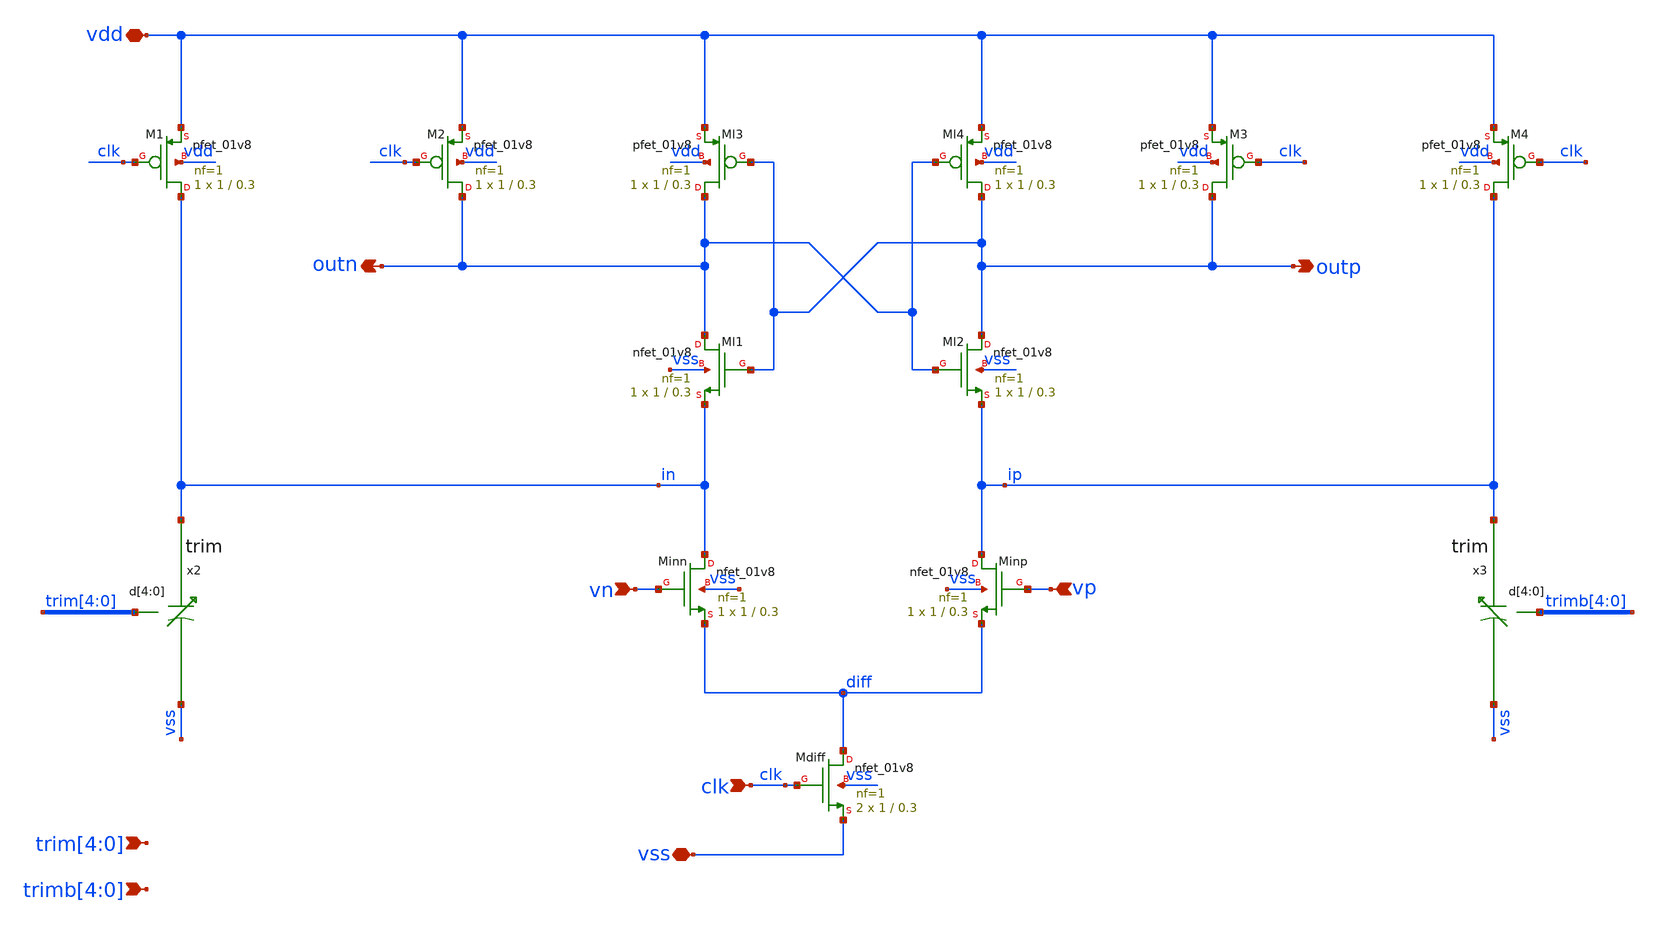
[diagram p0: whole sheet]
** sch_path: xschem/sar_10b/comparator/comparator.sch
**.subckt comparator vn vp clk vdd vss outp outn trim[4],trim[3],trim[2],trim[1],trim[0]
*+ trimb[4],trimb[3],trimb[2],trimb[1],trimb[0]
*.ipin vn
*.ipin vp
*.ipin clk
*.iopin vdd
*.iopin vss
*.opin outp
*.opin outn
*.ipin trim[4],trim[3],trim[2],trim[1],trim[0]
*.ipin trimb[4],trimb[3],trimb[2],trimb[1],trimb[0]
XMdiff diff clk vss vss sky130_fd_pr__nfet_01v8 L=0.3 W=1 nf=1 ad='int((nf+1)/2) * W/nf * 0.29' as='int((nf+2)/2) * W/nf * 0.29'
+ pd='2*int((nf+1)/2) * (W/nf + 0.29)' ps='2*int((nf+2)/2) * (W/nf + 0.29)' nrd='0.29 / W' nrs='0.29 / W'
+ sa=0 sb=0 sd=0 mult=2 m=2
XMinn in vn diff vss sky130_fd_pr__nfet_01v8 L=0.3 W=1 nf=1 ad='int((nf+1)/2) * W/nf * 0.29' as='int((nf+2)/2) * W/nf * 0.29'
+ pd='2*int((nf+1)/2) * (W/nf + 0.29)' ps='2*int((nf+2)/2) * (W/nf + 0.29)' nrd='0.29 / W' nrs='0.29 / W'
+ sa=0 sb=0 sd=0 mult=1 m=1
XMinp ip vp diff vss sky130_fd_pr__nfet_01v8 L=0.3 W=1 nf=1 ad='int((nf+1)/2) * W/nf * 0.29' as='int((nf+2)/2) * W/nf * 0.29'
+ pd='2*int((nf+1)/2) * (W/nf + 0.29)' ps='2*int((nf+2)/2) * (W/nf + 0.29)' nrd='0.29 / W' nrs='0.29 / W'
+ sa=0 sb=0 sd=0 mult=1 m=1
XMl4 outp outn vdd vdd sky130_fd_pr__pfet_01v8 L=0.3 W=1 nf=1 ad='int((nf+1)/2) * W/nf * 0.29' as='int((nf+2)/2) * W/nf * 0.29'
+ pd='2*int((nf+1)/2) * (W/nf + 0.29)' ps='2*int((nf+2)/2) * (W/nf + 0.29)' nrd='0.29 / W' nrs='0.29 / W'
+ sa=0 sb=0 sd=0 mult=1 m=1
XMl3 outn outp vdd vdd sky130_fd_pr__pfet_01v8 L=0.3 W=1 nf=1 ad='int((nf+1)/2) * W/nf * 0.29' as='int((nf+2)/2) * W/nf * 0.29'
+ pd='2*int((nf+1)/2) * (W/nf + 0.29)' ps='2*int((nf+2)/2) * (W/nf + 0.29)' nrd='0.29 / W' nrs='0.29 / W'
+ sa=0 sb=0 sd=0 mult=1 m=1
XM3 outp clk vdd vdd sky130_fd_pr__pfet_01v8 L=0.3 W=1 nf=1 ad='int((nf+1)/2) * W/nf * 0.29' as='int((nf+2)/2) * W/nf * 0.29'
+ pd='2*int((nf+1)/2) * (W/nf + 0.29)' ps='2*int((nf+2)/2) * (W/nf + 0.29)' nrd='0.29 / W' nrs='0.29 / W'
+ sa=0 sb=0 sd=0 mult=1 m=1
XM2 outn clk vdd vdd sky130_fd_pr__pfet_01v8 L=0.3 W=1 nf=1 ad='int((nf+1)/2) * W/nf * 0.29' as='int((nf+2)/2) * W/nf * 0.29'
+ pd='2*int((nf+1)/2) * (W/nf + 0.29)' ps='2*int((nf+2)/2) * (W/nf + 0.29)' nrd='0.29 / W' nrs='0.29 / W'
+ sa=0 sb=0 sd=0 mult=1 m=1
XMl1 outn outp in vss sky130_fd_pr__nfet_01v8 L=0.3 W=1 nf=1 ad='int((nf+1)/2) * W/nf * 0.29' as='int((nf+2)/2) * W/nf * 0.29'
+ pd='2*int((nf+1)/2) * (W/nf + 0.29)' ps='2*int((nf+2)/2) * (W/nf + 0.29)' nrd='0.29 / W' nrs='0.29 / W'
+ sa=0 sb=0 sd=0 mult=1 m=1
XMl2 outp outn ip vss sky130_fd_pr__nfet_01v8 L=0.3 W=1 nf=1 ad='int((nf+1)/2) * W/nf * 0.29' as='int((nf+2)/2) * W/nf * 0.29'
+ pd='2*int((nf+1)/2) * (W/nf + 0.29)' ps='2*int((nf+2)/2) * (W/nf + 0.29)' nrd='0.29 / W' nrs='0.29 / W'
+ sa=0 sb=0 sd=0 mult=1 m=1
XM4 ip clk vdd vdd sky130_fd_pr__pfet_01v8 L=0.3 W=1 nf=1 ad='int((nf+1)/2) * W/nf * 0.29' as='int((nf+2)/2) * W/nf * 0.29'
+ pd='2*int((nf+1)/2) * (W/nf + 0.29)' ps='2*int((nf+2)/2) * (W/nf + 0.29)' nrd='0.29 / W' nrs='0.29 / W'
+ sa=0 sb=0 sd=0 mult=1 m=1
XM1 in clk vdd vdd sky130_fd_pr__pfet_01v8 L=0.3 W=1 nf=1 ad='int((nf+1)/2) * W/nf * 0.29' as='int((nf+2)/2) * W/nf * 0.29'
+ pd='2*int((nf+1)/2) * (W/nf + 0.29)' ps='2*int((nf+2)/2) * (W/nf + 0.29)' nrd='0.29 / W' nrs='0.29 / W'
+ sa=0 sb=0 sd=0 mult=1 m=1
x2 in trim[4] trim[3] trim[2] trim[1] trim[0] vss trim
x3 ip trimb[4] trimb[3] trimb[2] trimb[1] trimb[0] vss trim
**.ends

* expanding   symbol:  sar_10b/comparator/trim.sym # of pins=3
** sym_path: xschem/sar_10b/comparator/trim.sym
** sch_path: xschem/sar_10b/comparator/trim.sch
.subckt trim drain d[4] d[3] d[2] d[1] d[0] vss
*.iopin vss
*.ipin d[4],d[3],d[2],d[1],d[0]
*.opin drain
XM4[7] n4 d[4] vss vss sky130_fd_pr__nfet_01v8_lvt L=0.3 W=1 nf=1 ad='int((nf+1)/2) * W/nf * 0.29' as='int((nf+2)/2) * W/nf * 0.29'
+ pd='2*int((nf+1)/2) * (W/nf + 0.29)' ps='2*int((nf+2)/2) * (W/nf + 0.29)' nrd='0.29 / W' nrs='0.29 / W'
+ sa=0 sb=0 sd=0 mult=1 m=1
XM4[6] n4 d[4] vss vss sky130_fd_pr__nfet_01v8_lvt L=0.3 W=1 nf=1 ad='int((nf+1)/2) * W/nf * 0.29' as='int((nf+2)/2) * W/nf * 0.29'
+ pd='2*int((nf+1)/2) * (W/nf + 0.29)' ps='2*int((nf+2)/2) * (W/nf + 0.29)' nrd='0.29 / W' nrs='0.29 / W'
+ sa=0 sb=0 sd=0 mult=1 m=1
XM4[5] n4 d[4] vss vss sky130_fd_pr__nfet_01v8_lvt L=0.3 W=1 nf=1 ad='int((nf+1)/2) * W/nf * 0.29' as='int((nf+2)/2) * W/nf * 0.29'
+ pd='2*int((nf+1)/2) * (W/nf + 0.29)' ps='2*int((nf+2)/2) * (W/nf + 0.29)' nrd='0.29 / W' nrs='0.29 / W'
+ sa=0 sb=0 sd=0 mult=1 m=1
XM4[4] n4 d[4] vss vss sky130_fd_pr__nfet_01v8_lvt L=0.3 W=1 nf=1 ad='int((nf+1)/2) * W/nf * 0.29' as='int((nf+2)/2) * W/nf * 0.29'
+ pd='2*int((nf+1)/2) * (W/nf + 0.29)' ps='2*int((nf+2)/2) * (W/nf + 0.29)' nrd='0.29 / W' nrs='0.29 / W'
+ sa=0 sb=0 sd=0 mult=1 m=1
XM4[3] n4 d[4] vss vss sky130_fd_pr__nfet_01v8_lvt L=0.3 W=1 nf=1 ad='int((nf+1)/2) * W/nf * 0.29' as='int((nf+2)/2) * W/nf * 0.29'
+ pd='2*int((nf+1)/2) * (W/nf + 0.29)' ps='2*int((nf+2)/2) * (W/nf + 0.29)' nrd='0.29 / W' nrs='0.29 / W'
+ sa=0 sb=0 sd=0 mult=1 m=1
XM4[2] n4 d[4] vss vss sky130_fd_pr__nfet_01v8_lvt L=0.3 W=1 nf=1 ad='int((nf+1)/2) * W/nf * 0.29' as='int((nf+2)/2) * W/nf * 0.29'
+ pd='2*int((nf+1)/2) * (W/nf + 0.29)' ps='2*int((nf+2)/2) * (W/nf + 0.29)' nrd='0.29 / W' nrs='0.29 / W'
+ sa=0 sb=0 sd=0 mult=1 m=1
XM4[1] n4 d[4] vss vss sky130_fd_pr__nfet_01v8_lvt L=0.3 W=1 nf=1 ad='int((nf+1)/2) * W/nf * 0.29' as='int((nf+2)/2) * W/nf * 0.29'
+ pd='2*int((nf+1)/2) * (W/nf + 0.29)' ps='2*int((nf+2)/2) * (W/nf + 0.29)' nrd='0.29 / W' nrs='0.29 / W'
+ sa=0 sb=0 sd=0 mult=1 m=1
XM4[0] n4 d[4] vss vss sky130_fd_pr__nfet_01v8_lvt L=0.3 W=1 nf=1 ad='int((nf+1)/2) * W/nf * 0.29' as='int((nf+2)/2) * W/nf * 0.29'
+ pd='2*int((nf+1)/2) * (W/nf + 0.29)' ps='2*int((nf+2)/2) * (W/nf + 0.29)' nrd='0.29 / W' nrs='0.29 / W'
+ sa=0 sb=0 sd=0 mult=1 m=1
XM3[3] n3 d[3] vss vss sky130_fd_pr__nfet_01v8_lvt L=0.3 W=1 nf=1 ad='int((nf+1)/2) * W/nf * 0.29' as='int((nf+2)/2) * W/nf * 0.29'
+ pd='2*int((nf+1)/2) * (W/nf + 0.29)' ps='2*int((nf+2)/2) * (W/nf + 0.29)' nrd='0.29 / W' nrs='0.29 / W'
+ sa=0 sb=0 sd=0 mult=1 m=1
XM3[2] n3 d[3] vss vss sky130_fd_pr__nfet_01v8_lvt L=0.3 W=1 nf=1 ad='int((nf+1)/2) * W/nf * 0.29' as='int((nf+2)/2) * W/nf * 0.29'
+ pd='2*int((nf+1)/2) * (W/nf + 0.29)' ps='2*int((nf+2)/2) * (W/nf + 0.29)' nrd='0.29 / W' nrs='0.29 / W'
+ sa=0 sb=0 sd=0 mult=1 m=1
XM3[1] n3 d[3] vss vss sky130_fd_pr__nfet_01v8_lvt L=0.3 W=1 nf=1 ad='int((nf+1)/2) * W/nf * 0.29' as='int((nf+2)/2) * W/nf * 0.29'
+ pd='2*int((nf+1)/2) * (W/nf + 0.29)' ps='2*int((nf+2)/2) * (W/nf + 0.29)' nrd='0.29 / W' nrs='0.29 / W'
+ sa=0 sb=0 sd=0 mult=1 m=1
XM3[0] n3 d[3] vss vss sky130_fd_pr__nfet_01v8_lvt L=0.3 W=1 nf=1 ad='int((nf+1)/2) * W/nf * 0.29' as='int((nf+2)/2) * W/nf * 0.29'
+ pd='2*int((nf+1)/2) * (W/nf + 0.29)' ps='2*int((nf+2)/2) * (W/nf + 0.29)' nrd='0.29 / W' nrs='0.29 / W'
+ sa=0 sb=0 sd=0 mult=1 m=1
XM2[1] n2 d[2] vss vss sky130_fd_pr__nfet_01v8_lvt L=0.3 W=1 nf=1 ad='int((nf+1)/2) * W/nf * 0.29' as='int((nf+2)/2) * W/nf * 0.29'
+ pd='2*int((nf+1)/2) * (W/nf + 0.29)' ps='2*int((nf+2)/2) * (W/nf + 0.29)' nrd='0.29 / W' nrs='0.29 / W'
+ sa=0 sb=0 sd=0 mult=1 m=1
XM2[0] n2 d[2] vss vss sky130_fd_pr__nfet_01v8_lvt L=0.3 W=1 nf=1 ad='int((nf+1)/2) * W/nf * 0.29' as='int((nf+2)/2) * W/nf * 0.29'
+ pd='2*int((nf+1)/2) * (W/nf + 0.29)' ps='2*int((nf+2)/2) * (W/nf + 0.29)' nrd='0.29 / W' nrs='0.29 / W'
+ sa=0 sb=0 sd=0 mult=1 m=1
XM1 n1 d[1] vss vss sky130_fd_pr__nfet_01v8_lvt L=0.3 W=1 nf=1 ad='int((nf+1)/2) * W/nf * 0.29' as='int((nf+2)/2) * W/nf * 0.29'
+ pd='2*int((nf+1)/2) * (W/nf + 0.29)' ps='2*int((nf+2)/2) * (W/nf + 0.29)' nrd='0.29 / W' nrs='0.29 / W'
+ sa=0 sb=0 sd=0 mult=1 m=1
XM0 n0 d[0] vss vss sky130_fd_pr__nfet_01v8_lvt L=0.3 W=1 nf=1 ad='int((nf+1)/2) * W/nf * 0.29' as='int((nf+2)/2) * W/nf * 0.29'
+ pd='2*int((nf+1)/2) * (W/nf + 0.29)' ps='2*int((nf+2)/2) * (W/nf + 0.29)' nrd='0.29 / W' nrs='0.29 / W'
+ sa=0 sb=0 sd=0 mult=1 m=1
x4[7] drain n4 trimcap
x4[6] drain n4 trimcap
x4[5] drain n4 trimcap
x4[4] drain n4 trimcap
x4[3] drain n4 trimcap
x4[2] drain n4 trimcap
x4[1] drain n4 trimcap
x4[0] drain n4 trimcap
x3[3] drain n3 trimcap
x3[2] drain n3 trimcap
x3[1] drain n3 trimcap
x3[0] drain n3 trimcap
x2[1] drain n2 trimcap
x2[0] drain n2 trimcap
x1 drain n1 trimcap
x0 drain n0 trimcap
.ends


* expanding   symbol:  sar_10b/comparator/trimcap.sym # of pins=2
** sym_path: xschem/sar_10b/comparator/trimcap.sym
** sch_path: xschem/sar_10b/comparator/trimcap.sch
.subckt trimcap cp cn
*.iopin cp
*.iopin cn
c0 net1 cn 2f m=1
c1 cp net1 1f m=1
.ends

.end
